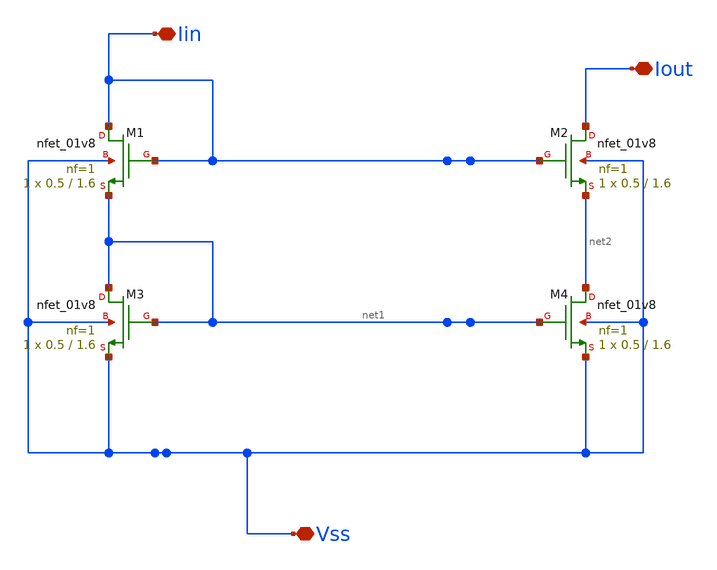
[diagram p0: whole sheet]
** sch_path: xschem/ccm_nmos_tt.sch
**.subckt ccm_nmos_tt Vss Iin Iout
*.iopin Vss
*.iopin Iin
*.iopin Iout
XM3 net1 net1 Vss Vss sky130_fd_pr__nfet_01v8 L=1.6 W=0.5 nf=1 ad='int((1 + 1)/2) * 0.5 / 1 * 0.29' as='int((1 + 2)/2) * 0.5 / 1 * 0.29'
+ pd='2*int((1 + 1)/2) * (0.5 / 1 + 0.29)' ps='2*int((1 + 2)/2) * (0.5 / 1 + 0.29)' nrd='0.29 / 0.5 ' nrs='0.29 / 0.5 '
+ sa=0 sb=0 sd=0 mult=1 m=1
XM4 net2 net1 Vss Vss sky130_fd_pr__nfet_01v8 L=1.6 W=0.5 nf=1 ad='int((1 + 1)/2) * 0.5 / 1 * 0.29' as='int((1 + 2)/2) * 0.5 / 1 * 0.29'
+ pd='2*int((1 + 1)/2) * (0.5 / 1 + 0.29)' ps='2*int((1 + 2)/2) * (0.5 / 1 + 0.29)' nrd='0.29 / 0.5 ' nrs='0.29 / 0.5 '
+ sa=0 sb=0 sd=0 mult=1 m=1
XM1 Iin Iin net1 Vss sky130_fd_pr__nfet_01v8 L=1.6 W=0.5 nf=1 ad='int((1 + 1)/2) * 0.5 / 1 * 0.29' as='int((1 + 2)/2) * 0.5 / 1 * 0.29'
+ pd='2*int((1 + 1)/2) * (0.5 / 1 + 0.29)' ps='2*int((1 + 2)/2) * (0.5 / 1 + 0.29)' nrd='0.29 / 0.5 ' nrs='0.29 / 0.5 '
+ sa=0 sb=0 sd=0 mult=1 m=1
XM2 Iout Iin net2 Vss sky130_fd_pr__nfet_01v8 L=1.6 W=0.5 nf=1 ad='int((1 + 1)/2) * 0.5 / 1 * 0.29' as='int((1 + 2)/2) * 0.5 / 1 * 0.29'
+ pd='2*int((1 + 1)/2) * (0.5 / 1 + 0.29)' ps='2*int((1 + 2)/2) * (0.5 / 1 + 0.29)' nrd='0.29 / 0.5 ' nrs='0.29 / 0.5 '
+ sa=0 sb=0 sd=0 mult=1 m=1
**.ends
.end
